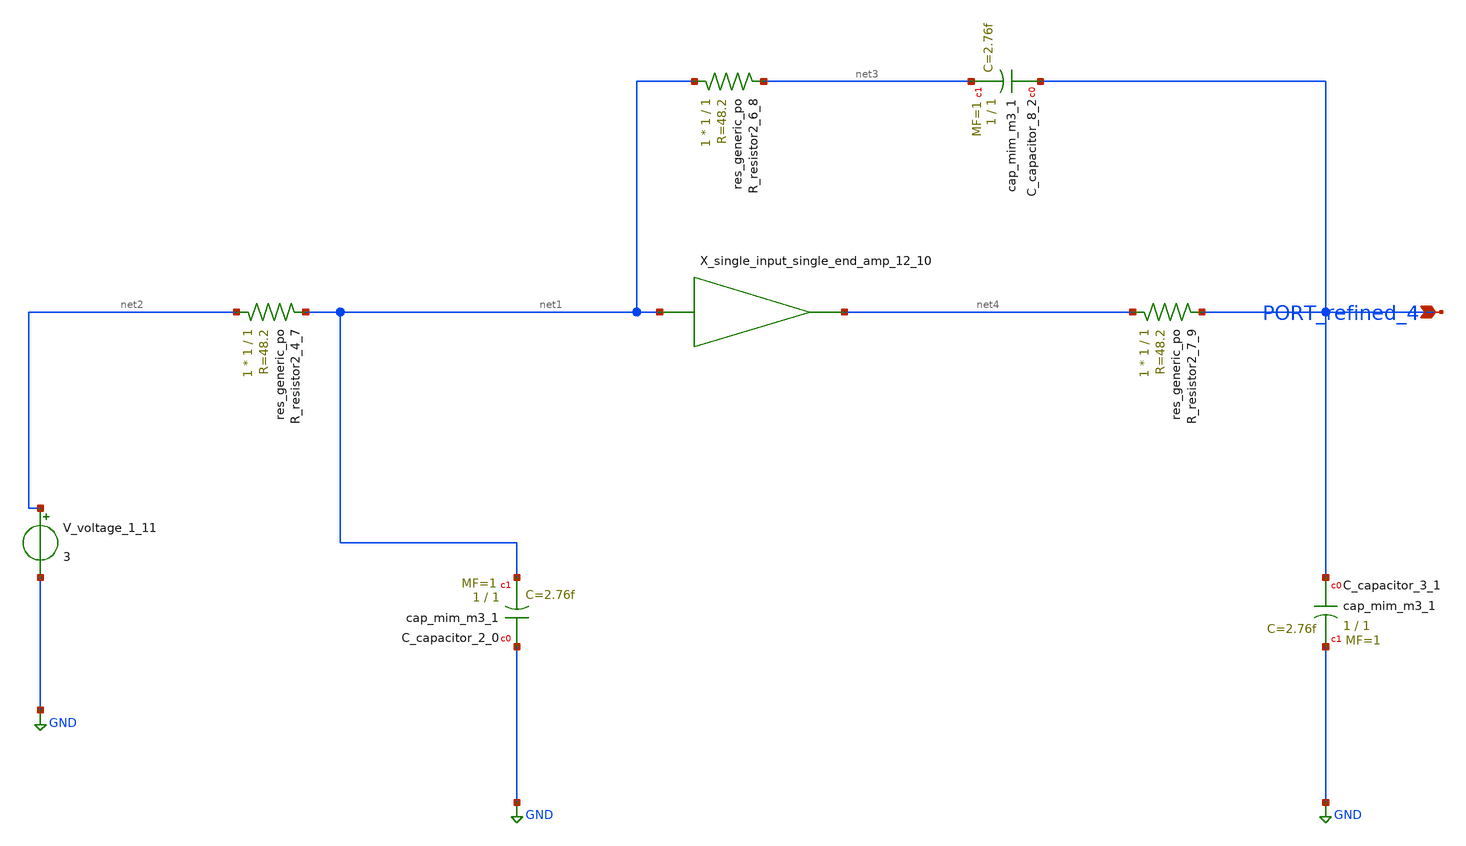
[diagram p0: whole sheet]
** sch_path: schematics/AMSNet/359.sch
**.subckt 359 PORT_refined_4
*.ipin PORT_refined_4
XC_capacitor_2_0 GND net1 sky130_fd_pr__cap_mim_m3_1 W=1 L=1 MF=1 m=1
XC_capacitor_3_1 PORT_refined_4 GND sky130_fd_pr__cap_mim_m3_1 W=1 L=1 MF=1 m=1
XC_capacitor_8_2 PORT_refined_4 net3 sky130_fd_pr__cap_mim_m3_1 W=1 L=1 MF=1 m=1
XR_resistor2_4_7 net2 net1 sky130_fd_pr__res_generic_po W=1 L=1 m=1
XR_resistor2_6_8 net1 net3 sky130_fd_pr__res_generic_po W=1 L=1 m=1
XR_resistor2_7_9 net4 PORT_refined_4 sky130_fd_pr__res_generic_po W=1 L=1 m=1
X_single_input_single_end_amp_12_10 net1 net4 schemgen_siso_amp
V_voltage_1_11 net2 GND 3
**.ends

* expanding   symbol:  schemgen_siso_amp.sym # of pins=2
** sym_path: symbols/schemgen_siso_amp.sym
.subckt schemgen_siso_amp IN OUT
* SchemGen ideal single-input amplifier: Vout = 1e5 * V(IN)
E1 OUT 0 IN 0 1e5
.ends schemgen_siso_amp
.GLOBAL GND
.end
